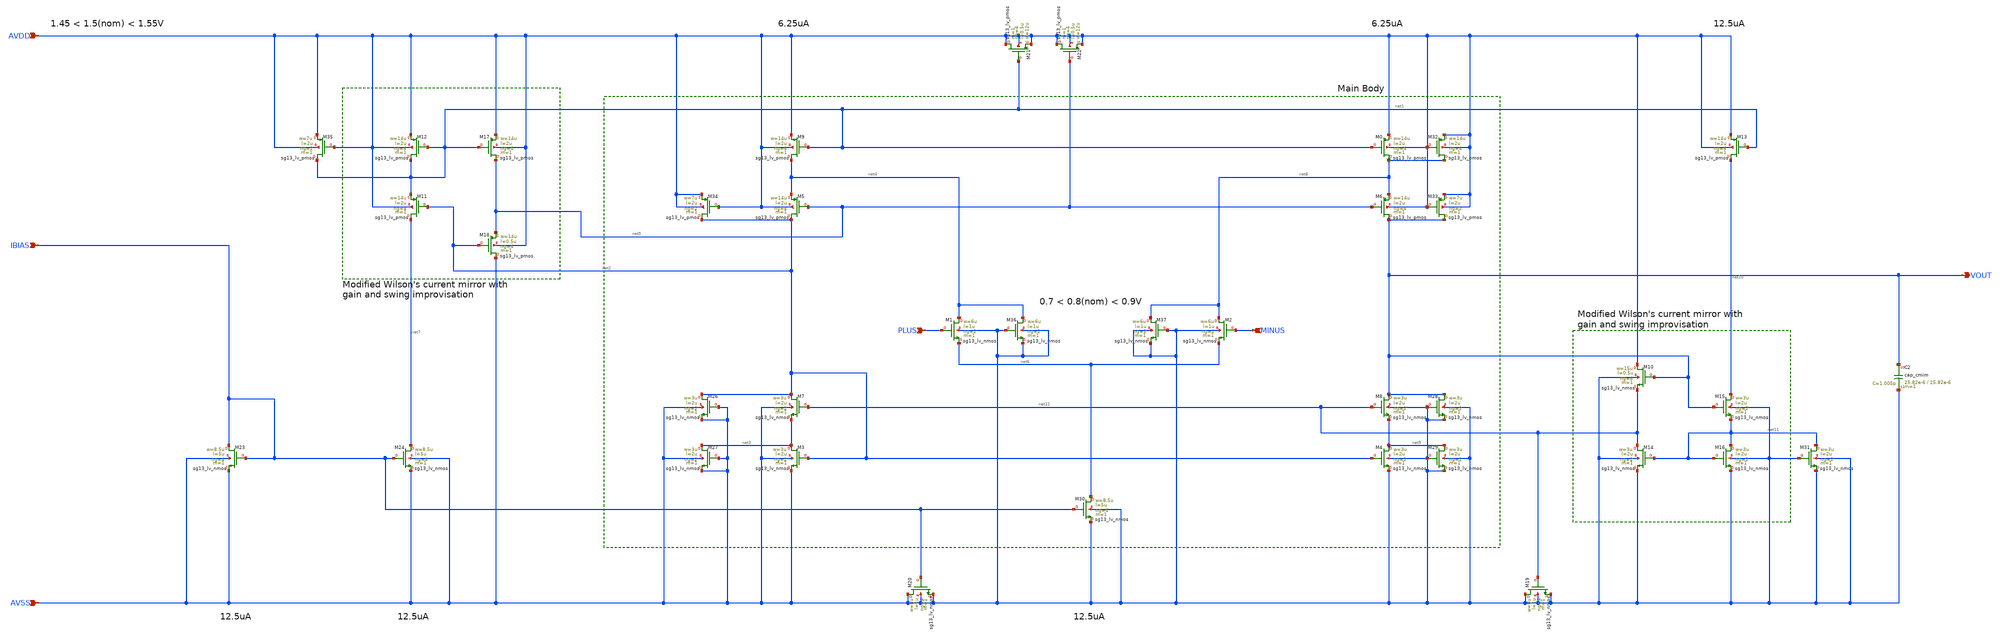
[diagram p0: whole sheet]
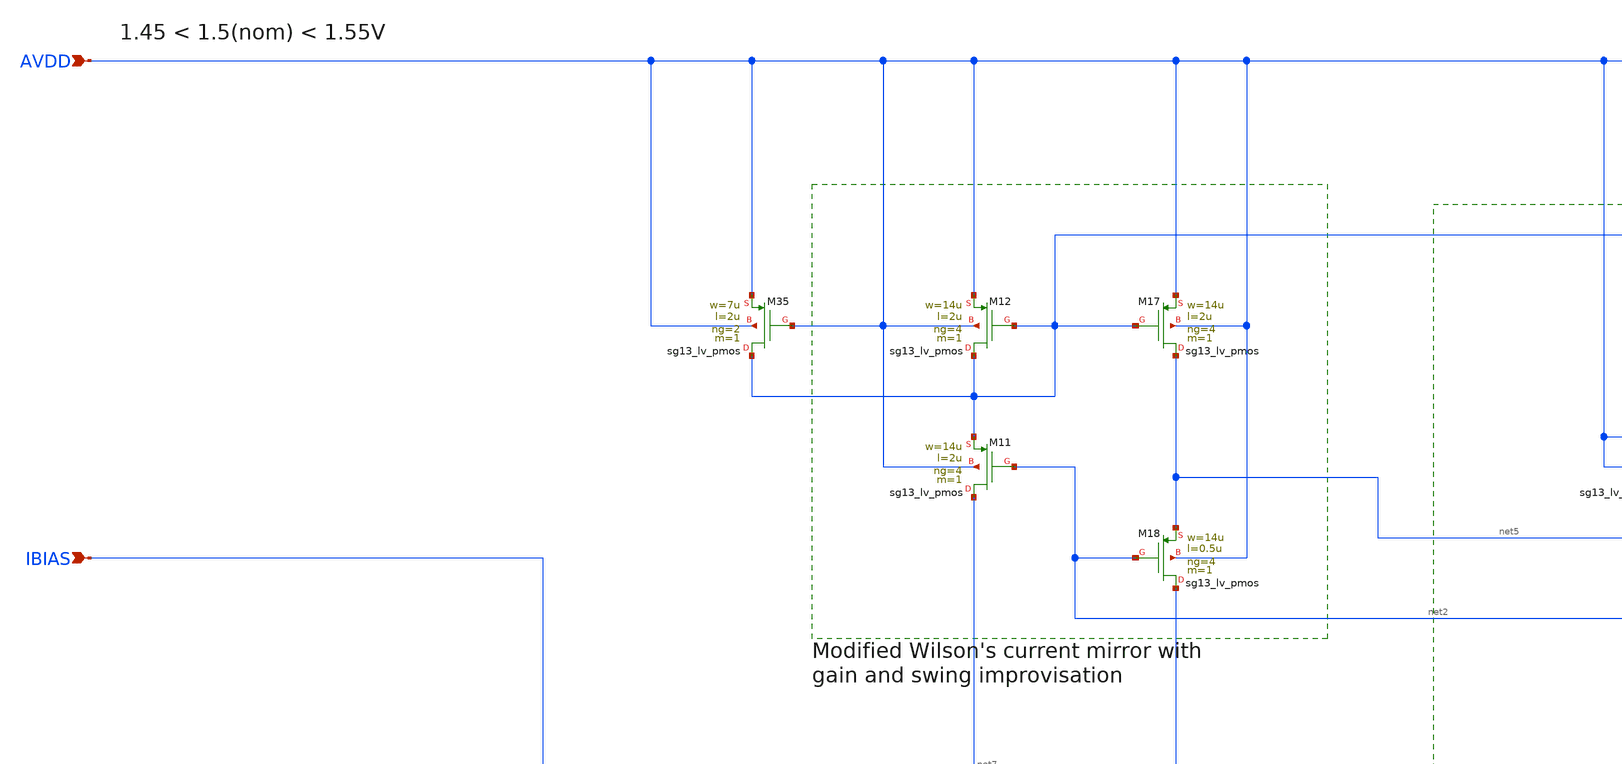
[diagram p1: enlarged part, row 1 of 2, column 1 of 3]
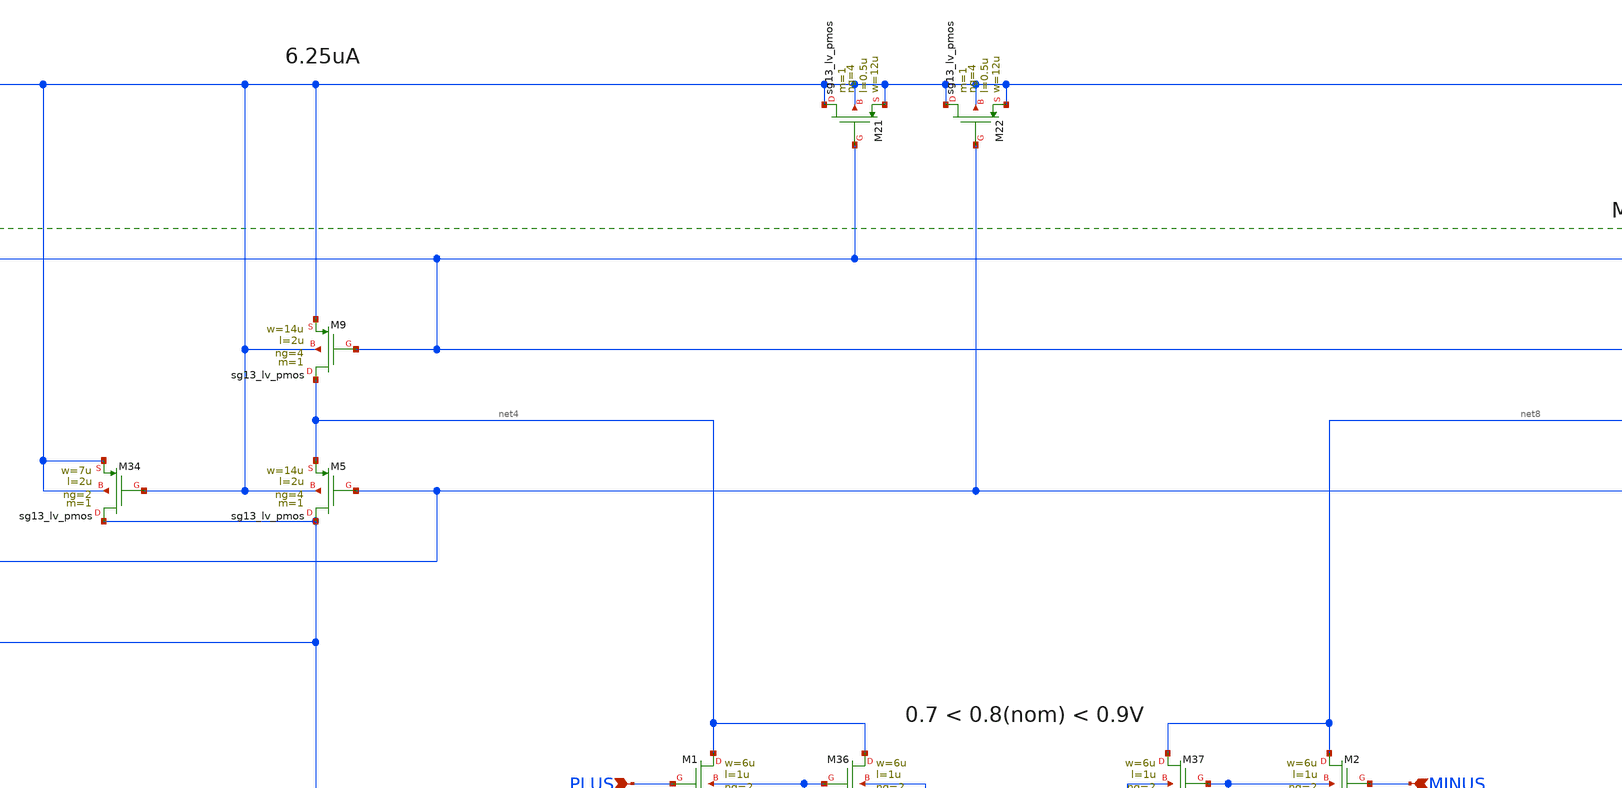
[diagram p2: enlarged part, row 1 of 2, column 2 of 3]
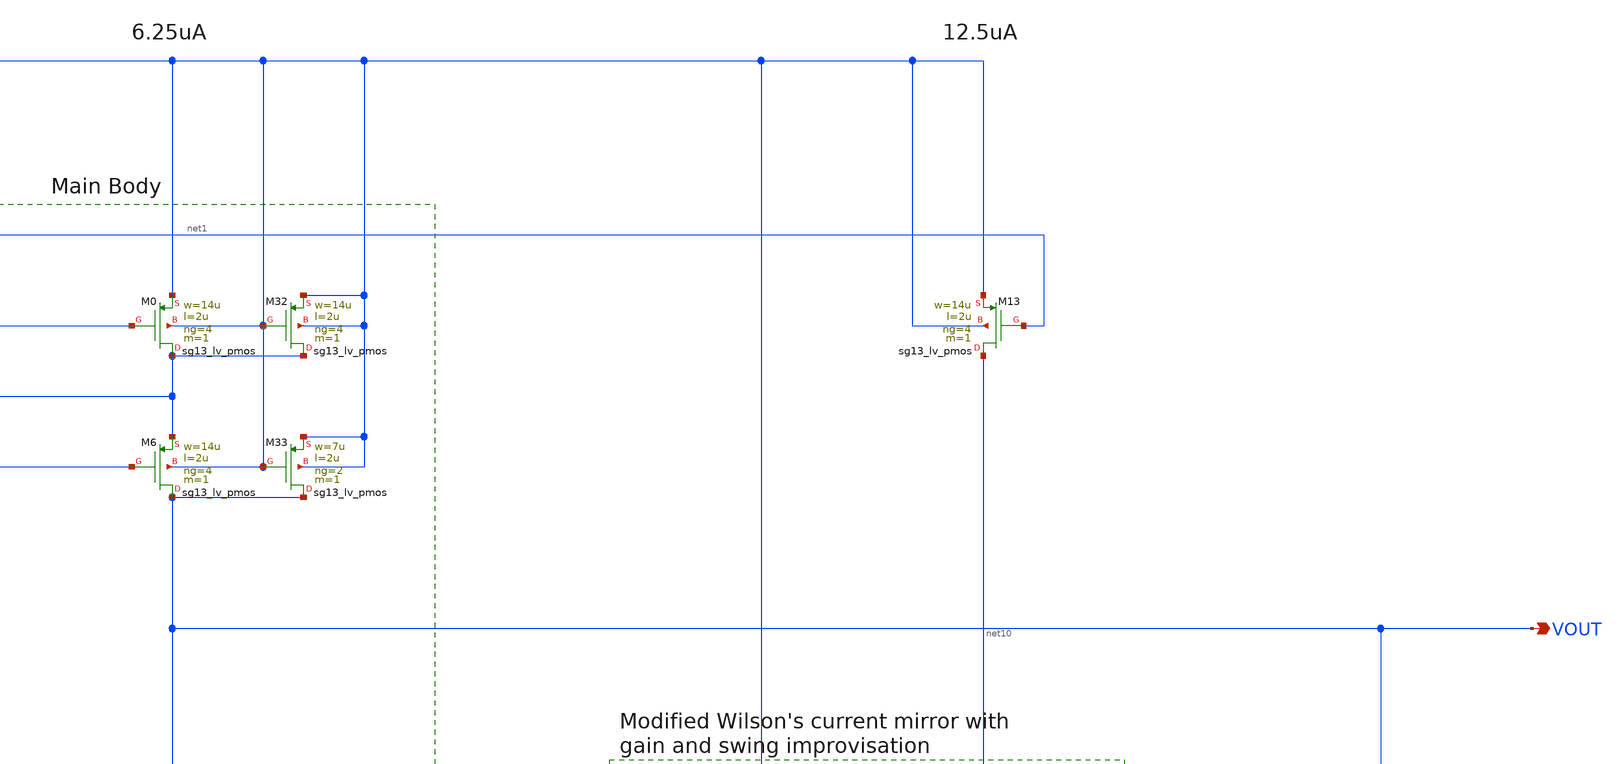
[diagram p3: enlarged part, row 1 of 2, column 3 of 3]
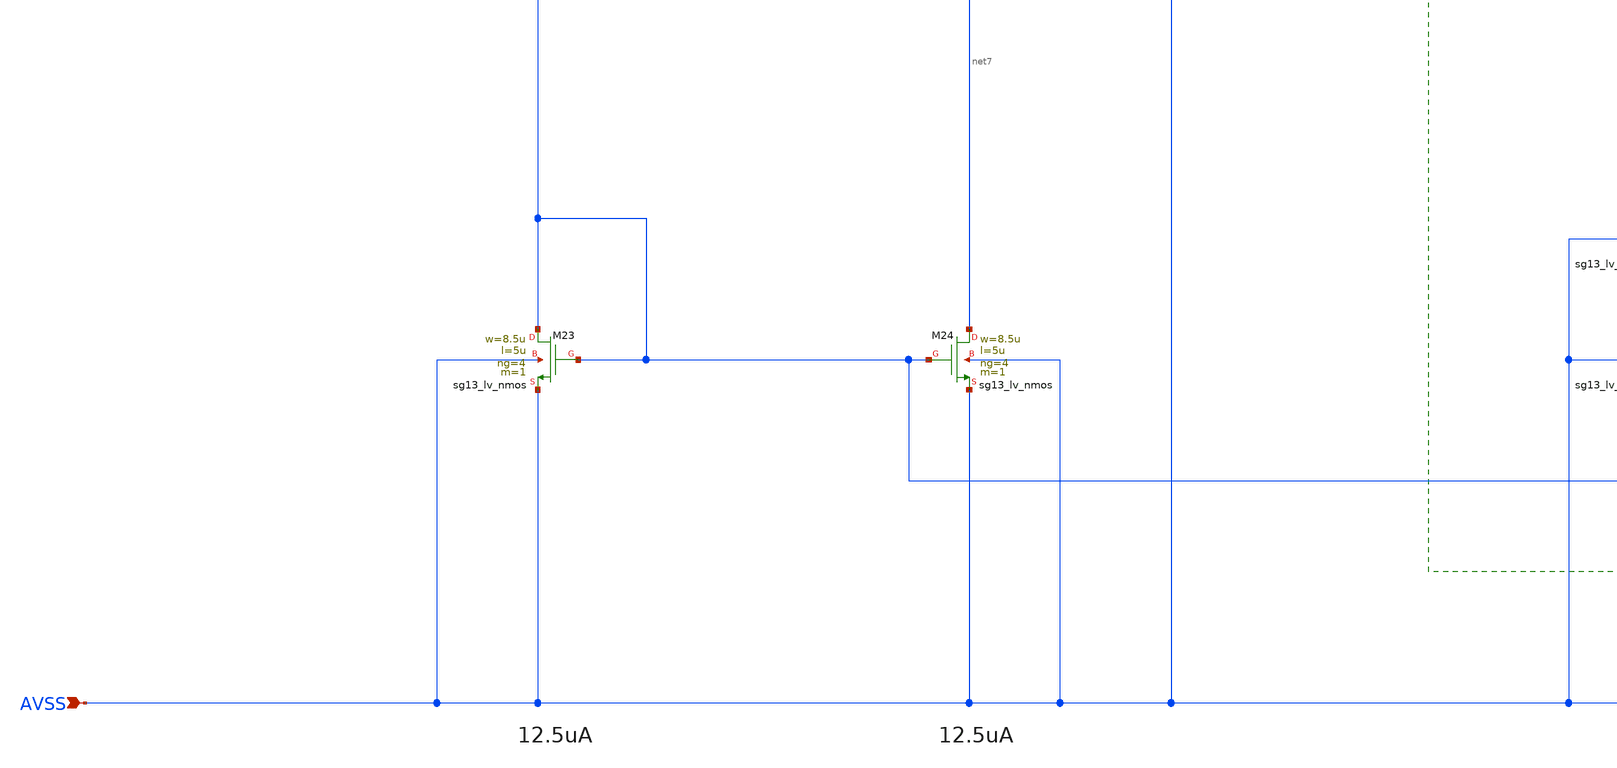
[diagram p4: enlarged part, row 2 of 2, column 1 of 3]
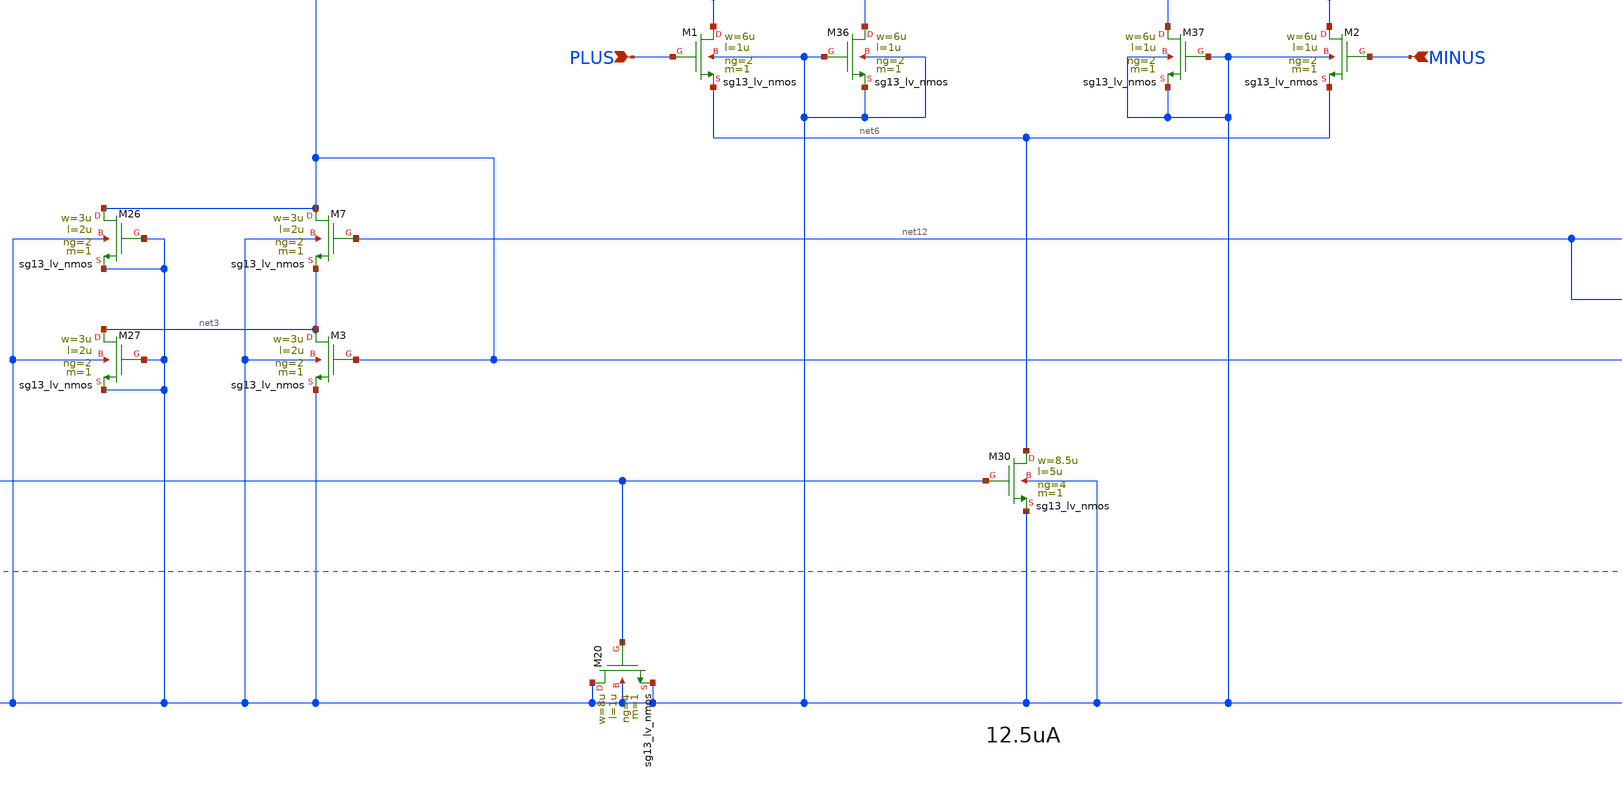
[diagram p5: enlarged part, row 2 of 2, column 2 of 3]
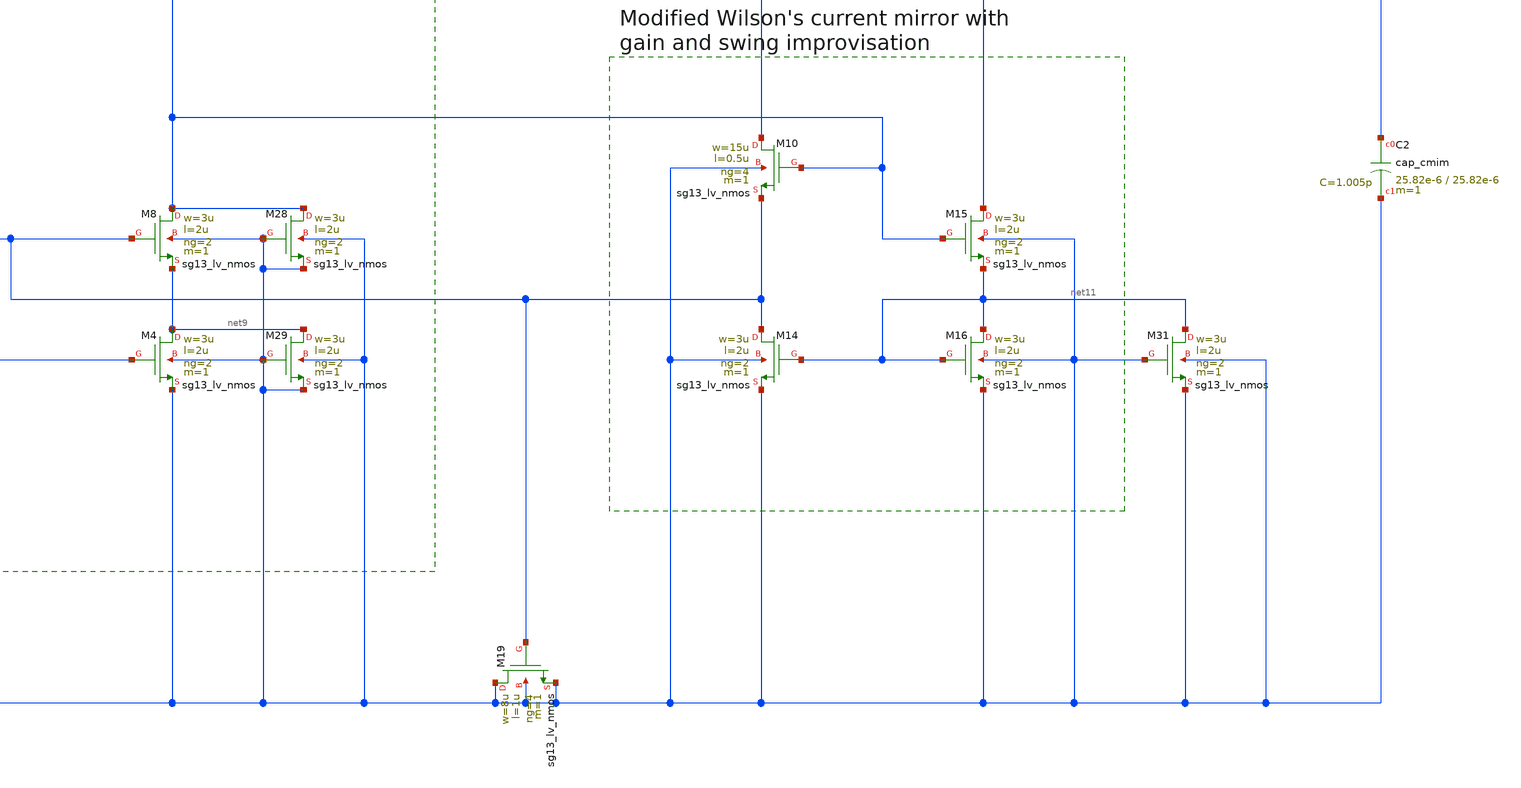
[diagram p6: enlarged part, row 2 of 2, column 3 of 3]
** sch_path: Designs/otas/1_schematics/ota_final_decoup.sch
* (c) 2025 Thesis_HP, Apache-2.0 license
**.subckt ota_final_decoup AVSS IBIAS AVDD PLUS MINUS VOUT
*.ipin AVSS
*.ipin IBIAS
*.ipin AVDD
*.ipin PLUS
*.ipin MINUS
*.opin VOUT
XM23 IBIAS IBIAS AVSS AVSS sg13_lv_nmos w=8.5u l=5u ng=4 m=1 mm_ok=1
XM24 net7 IBIAS AVSS AVSS sg13_lv_nmos w=8.5u l=5u ng=4 m=1 mm_ok=1
XM11 net7 net2 net1 AVDD sg13_lv_pmos w=14u l=2u ng=4 m=1 mm_ok=1
XM12 net1 net1 AVDD AVDD sg13_lv_pmos w=14u l=2u ng=4 m=1 mm_ok=1
XM18 AVSS net2 net5 AVDD sg13_lv_pmos w=14u l=0.5u ng=4 m=1 mm_ok=1
XM17 net5 net1 AVDD AVDD sg13_lv_pmos w=14u l=2u ng=4 m=1 mm_ok=1
XM9 net4 net1 AVDD AVDD sg13_lv_pmos w=14u l=2u ng=4 m=1 mm_ok=1
XM5 net2 net5 net4 AVDD sg13_lv_pmos w=14u l=2u ng=4 m=1 mm_ok=1
XM7 net2 net12 net3 AVSS sg13_lv_nmos w=3u l=2u ng=2 m=1 mm_ok=1
XM3 net3 net2 AVSS AVSS sg13_lv_nmos w=3u l=2u ng=2 m=1 mm_ok=1
XM30 net6 IBIAS AVSS AVSS sg13_lv_nmos w=8.5u l=5u ng=4 m=1 mm_ok=1
XM1 net4 PLUS net6 AVSS sg13_lv_nmos w=6u l=1u ng=2 m=1 mm_ok=1
XM2 net8 MINUS net6 AVSS sg13_lv_nmos w=6u l=1u ng=2 m=1 mm_ok=1
XM37 net8 AVSS AVSS AVSS sg13_lv_nmos w=6u l=1u ng=2 m=1 mm_ok=1
XM6 VOUT net5 net8 AVDD sg13_lv_pmos w=14u l=2u ng=4 m=1 mm_ok=1
XM0 net8 net1 AVDD AVDD sg13_lv_pmos w=14u l=2u ng=4 m=1 mm_ok=1
XM8 VOUT net12 net9 AVSS sg13_lv_nmos w=3u l=2u ng=2 m=1 mm_ok=1
XM4 net9 net2 AVSS AVSS sg13_lv_nmos w=3u l=2u ng=2 m=1 mm_ok=1
XM29 net9 AVSS AVSS AVSS sg13_lv_nmos w=3u l=2u ng=2 m=1 mm_ok=1
XM28 VOUT AVSS AVSS AVSS sg13_lv_nmos w=3u l=2u ng=2 m=1 mm_ok=1
XM32 net8 AVDD AVDD AVDD sg13_lv_pmos w=14u l=2u ng=4 m=1 mm_ok=1
XM33 VOUT AVDD AVDD AVDD sg13_lv_pmos w=7u l=2u ng=2 m=1 mm_ok=1
XM13 net10 net1 AVDD AVDD sg13_lv_pmos w=14u l=2u ng=4 m=1 mm_ok=1
XM15 net10 VOUT net11 AVSS sg13_lv_nmos w=3u l=2u ng=2 m=1 mm_ok=1
XM16 net11 net11 AVSS AVSS sg13_lv_nmos w=3u l=2u ng=2 m=1 mm_ok=1
XM14 net12 net11 AVSS AVSS sg13_lv_nmos w=3u l=2u ng=2 m=1 mm_ok=1
XM10 AVDD VOUT net12 AVSS sg13_lv_nmos w=15u l=0.5u ng=4 m=1 mm_ok=1
XM36 net4 AVSS AVSS AVSS sg13_lv_nmos w=6u l=1u ng=2 m=1 mm_ok=1
XM34 net2 AVDD AVDD AVDD sg13_lv_pmos w=7u l=2u ng=2 m=1 mm_ok=1
XM27 net3 AVSS AVSS AVSS sg13_lv_nmos w=3u l=2u ng=2 m=1 mm_ok=1
XM26 net2 AVSS AVSS AVSS sg13_lv_nmos w=3u l=2u ng=2 m=1 mm_ok=1
XM35 net1 AVDD AVDD AVDD sg13_lv_pmos w=7u l=2u ng=2 m=1 mm_ok=1
XM31 net11 AVSS AVSS AVSS sg13_lv_nmos w=3u l=2u ng=2 m=1 mm_ok=1
XC2 VOUT AVSS cap_cmim w=25.82e-6 l=25.82e-6 m=1 mm_ok=1
XM19 AVSS net12 AVSS AVSS sg13_lv_nmos w=8u l=1u ng=4 m=1 mm_ok=1
XM20 AVSS IBIAS AVSS AVSS sg13_lv_nmos w=8u l=1u ng=4 m=1 mm_ok=1
XM21 AVDD net1 AVDD AVDD sg13_lv_pmos w=12u l=0.5u ng=4 m=1 mm_ok=1
XM22 AVDD net5 AVDD AVDD sg13_lv_pmos w=12u l=0.5u ng=4 m=1 mm_ok=1
**.ends
.end
